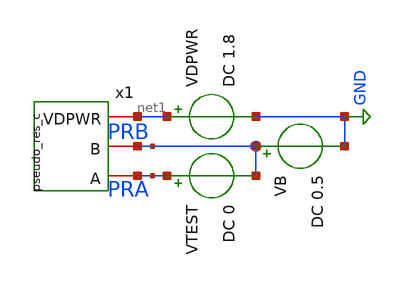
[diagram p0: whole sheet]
** sch_path: xschem/tb_psuedo_res_c.sch
**.subckt tb_psuedo_res_c
x1 net1 PRB PRA pseudo_res_c
VDPWR net1 GND DC 1.8
VTEST PRA PRB DC 0
VB PRB GND DC 0.5
**** begin user architecture code


.lib /foss/pdks/sky130A/libs.tech/ngspice/sky130.lib.spice tt
.option savecurrents
.temp 27

.control
save all

dc VTEST -0.5 0.5 0.005

* Current through test source
plot -i(vtest)
plot abs(-i(vtest)) ylog

* Effective resistance
let z_eff = abs(v(pra,prb) / vtest#branch)

plot z_eff ylog

print z_eff[100]

.endc


**** end user architecture code
**.ends

* expanding   symbol:  pseudo_res_c.sym # of pins=3
** sym_path: xschem/pseudo_res_c.sym
** sch_path: xschem/pseudo_res_c.sch
.subckt pseudo_res_c VDPWR B A
*.iopin A
*.iopin B
*.iopin VDPWR
XP1 A net1 net1 VDPWR sky130_fd_pr__pfet_01v8 L=5 W=0.5 nf=1 ad='int((1 + 1)/2) * 0.5 / 1 * 0.29' as='int((1 + 2)/2) * 0.5 / 1 * 0.29'
+ pd='2*int((1 + 1)/2) * (0.5 / 1 + 0.29)' ps='2*int((1 + 2)/2) * (0.5 / 1 + 0.29)' nrd='0.29 / 0.5 ' nrs='0.29 / 0.5 '
+ sa=0 sb=0 sd=0 mult=10 m=10
XP2 net1 net1 B VDPWR sky130_fd_pr__pfet_01v8 L=5 W=0.5 nf=1 ad='int((1 + 1)/2) * 0.5 / 1 * 0.29' as='int((1 + 2)/2) * 0.5 / 1 * 0.29'
+ pd='2*int((1 + 1)/2) * (0.5 / 1 + 0.29)' ps='2*int((1 + 2)/2) * (0.5 / 1 + 0.29)' nrd='0.29 / 0.5 ' nrs='0.29 / 0.5 '
+ sa=0 sb=0 sd=0 mult=10 m=10
.ends

.GLOBAL GND
.end
